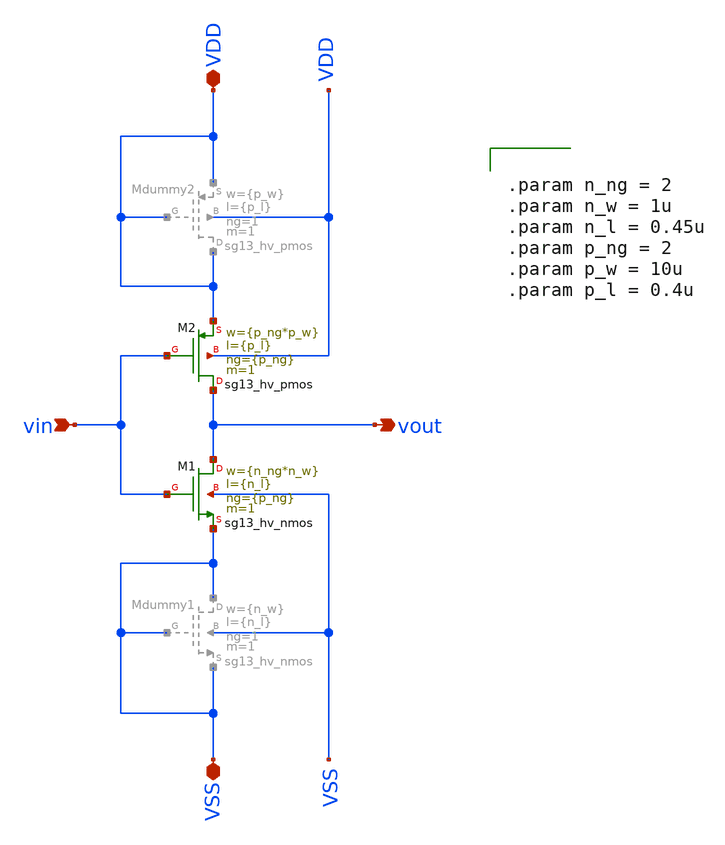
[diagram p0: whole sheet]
** sch_path: macros/heichips26_vcr/macros/switched_capacitor/schematic/xschem/high_th_inverter.sch
**.subckt high_th_inverter vin VDD VSS vout
*.ipin vin
*.iopin VDD
*.iopin VSS
*.opin vout
XM1 vout vin VSS VSS sg13_hv_nmos w={n_ng*n_w} l={n_l} ng={p_ng} m=1 mm_ok=1
XM2 vout vin VDD VDD sg13_hv_pmos w={p_ng*p_w} l={p_l} ng={p_ng} m=1 mm_ok=1
**** begin user architecture code


.param n_ng = 2
.param n_w = 1u
.param n_l = 0.45u
.param p_ng = 2
.param p_w = 10u
.param p_l = 0.4u


**** end user architecture code
**.ends
.end
